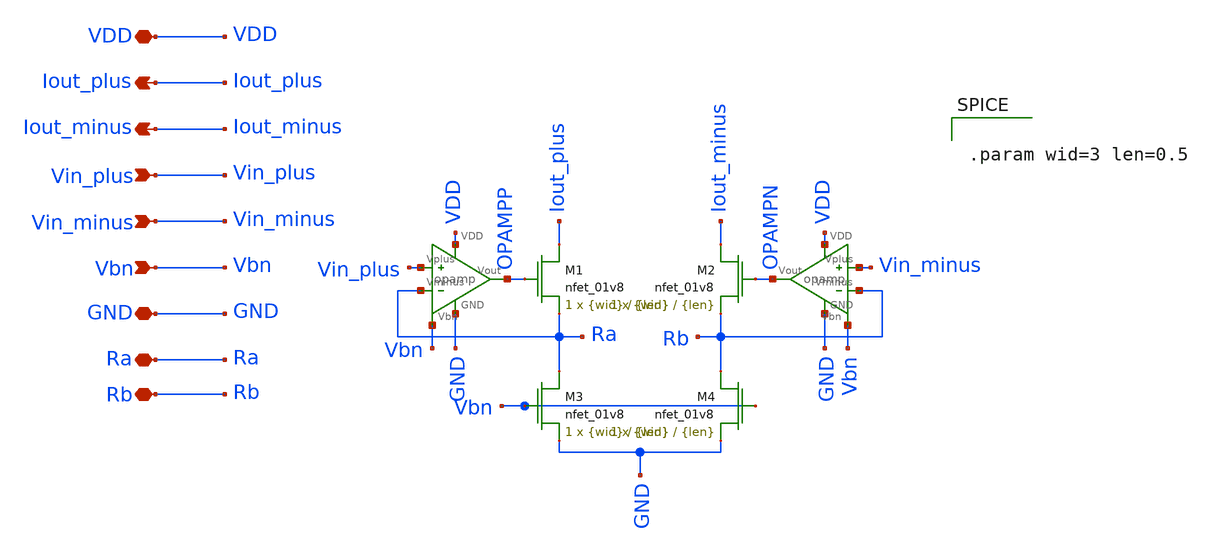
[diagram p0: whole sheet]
** sch_path: final/schematics/VI_input.sch
**.subckt VI_input Iout_plus Iout_minus VDD Vin_plus Vin_minus Vbn GND Ra Rb
*.opin Iout_plus
*.opin Iout_minus
*.iopin VDD
*.ipin Vin_plus
*.ipin Vin_minus
*.ipin Vbn
*.iopin GND
*.iopin Ra
*.iopin Rb
X2 OPAMPN VDD GND Vin_minus Rb Vbn opamp
XM4 Rb Vbn GND GND sky130_fd_pr__nfet_01v8 L={len} W={wid} nf=1 ad='int((nf+1)/2) * W/nf * 0.29' as='int((nf+2)/2) * W/nf * 0.29'
+ pd='2*int((nf+1)/2) * (W/nf + 0.29)' ps='2*int((nf+2)/2) * (W/nf + 0.29)' nrd='0.29 / W' nrs='0.29 / W'
+ sa=0 sb=0 sd=0 mult=1 m=1
X1 OPAMPP VDD GND Vin_plus Ra Vbn opamp
XM3 Ra Vbn GND GND sky130_fd_pr__nfet_01v8 L={len} W={wid} nf=1 ad='int((nf+1)/2) * W/nf * 0.29' as='int((nf+2)/2) * W/nf * 0.29'
+ pd='2*int((nf+1)/2) * (W/nf + 0.29)' ps='2*int((nf+2)/2) * (W/nf + 0.29)' nrd='0.29 / W' nrs='0.29 / W'
+ sa=0 sb=0 sd=0 mult=1 m=1
XM1 Iout_plus OPAMPP Ra GND sky130_fd_pr__nfet_01v8 L={len} W={wid} nf=1 ad='int((nf+1)/2) * W/nf * 0.29'
+ as='int((nf+2)/2) * W/nf * 0.29' pd='2*int((nf+1)/2) * (W/nf + 0.29)' ps='2*int((nf+2)/2) * (W/nf + 0.29)'
+ nrd='0.29 / W' nrs='0.29 / W' sa=0 sb=0 sd=0 mult=1 m=1
XM2 Iout_minus OPAMPN Rb GND sky130_fd_pr__nfet_01v8 L={len} W={wid} nf=1 ad='int((nf+1)/2) * W/nf * 0.29'
+ as='int((nf+2)/2) * W/nf * 0.29' pd='2*int((nf+1)/2) * (W/nf + 0.29)' ps='2*int((nf+2)/2) * (W/nf + 0.29)'
+ nrd='0.29 / W' nrs='0.29 / W' sa=0 sb=0 sd=0 mult=1 m=1
**** begin user architecture code


.param wid=3 len=0.5


**** end user architecture code
**.ends

* expanding   symbol:  opamp.sym # of pins=6
** sym_path: final/schematics/opamp.sym
** sch_path: final/schematics/opamp.sch
.subckt opamp Vout VDD GND Vplus Vminus Vbn
*.iopin VDD
*.iopin GND
*.ipin Vplus
*.ipin Vminus
*.opin Vout
*.ipin Vbn
XM3 net2 Vbn GND GND sky130_fd_pr__nfet_01v8 L={len} W={wid} nf=1 ad='int((nf+1)/2) * W/nf * 0.29' as='int((nf+2)/2) * W/nf * 0.29'
+ pd='2*int((nf+1)/2) * (W/nf + 0.29)' ps='2*int((nf+2)/2) * (W/nf + 0.29)' nrd='0.29 / W' nrs='0.29 / W'
+ sa=0 sb=0 sd=0 mult=1 m=1
XM4 net1 net1 VDD VDD sky130_fd_pr__pfet_01v8 L={len} W={wid} nf=1 ad='int((nf+1)/2) * W/nf * 0.29' as='int((nf+2)/2) * W/nf * 0.29'
+ pd='2*int((nf+1)/2) * (W/nf + 0.29)' ps='2*int((nf+2)/2) * (W/nf + 0.29)' nrd='0.29 / W' nrs='0.29 / W'
+ sa=0 sb=0 sd=0 mult=1 m=1
XM5 Vout net1 VDD VDD sky130_fd_pr__pfet_01v8 L={len} W={wid} nf=1 ad='int((nf+1)/2) * W/nf * 0.29' as='int((nf+2)/2) * W/nf * 0.29'
+ pd='2*int((nf+1)/2) * (W/nf + 0.29)' ps='2*int((nf+2)/2) * (W/nf + 0.29)' nrd='0.29 / W' nrs='0.29 / W'
+ sa=0 sb=0 sd=0 mult=1 m=1
XM1 net1 Vplus net2 GND sky130_fd_pr__nfet_01v8 L={len} W={wid} nf=1 ad='int((nf+1)/2) * W/nf * 0.29'
+ as='int((nf+2)/2) * W/nf * 0.29' pd='2*int((nf+1)/2) * (W/nf + 0.29)' ps='2*int((nf+2)/2) * (W/nf + 0.29)'
+ nrd='0.29 / W' nrs='0.29 / W' sa=0 sb=0 sd=0 mult=1 m=1
XM2 Vout Vminus net2 GND sky130_fd_pr__nfet_01v8 L={len} W={wid} nf=1 ad='int((nf+1)/2) * W/nf * 0.29'
+ as='int((nf+2)/2) * W/nf * 0.29' pd='2*int((nf+1)/2) * (W/nf + 0.29)' ps='2*int((nf+2)/2) * (W/nf + 0.29)'
+ nrd='0.29 / W' nrs='0.29 / W' sa=0 sb=0 sd=0 mult=1 m=1
**** begin user architecture code


.param wid=3 len=0.5


**** end user architecture code
.ends

.end
